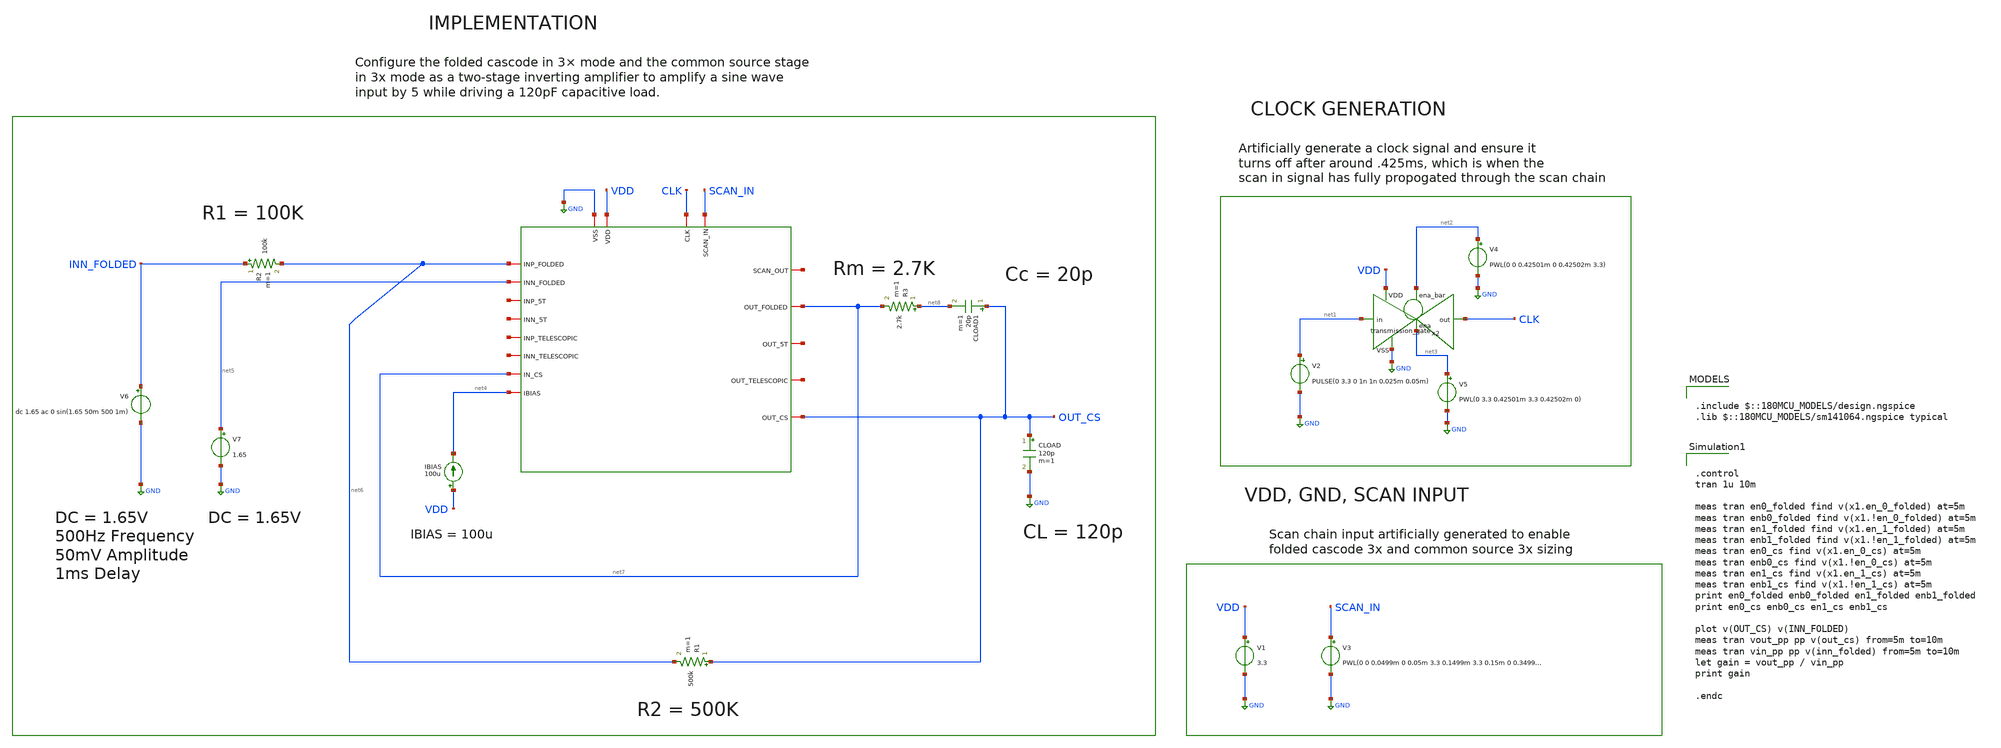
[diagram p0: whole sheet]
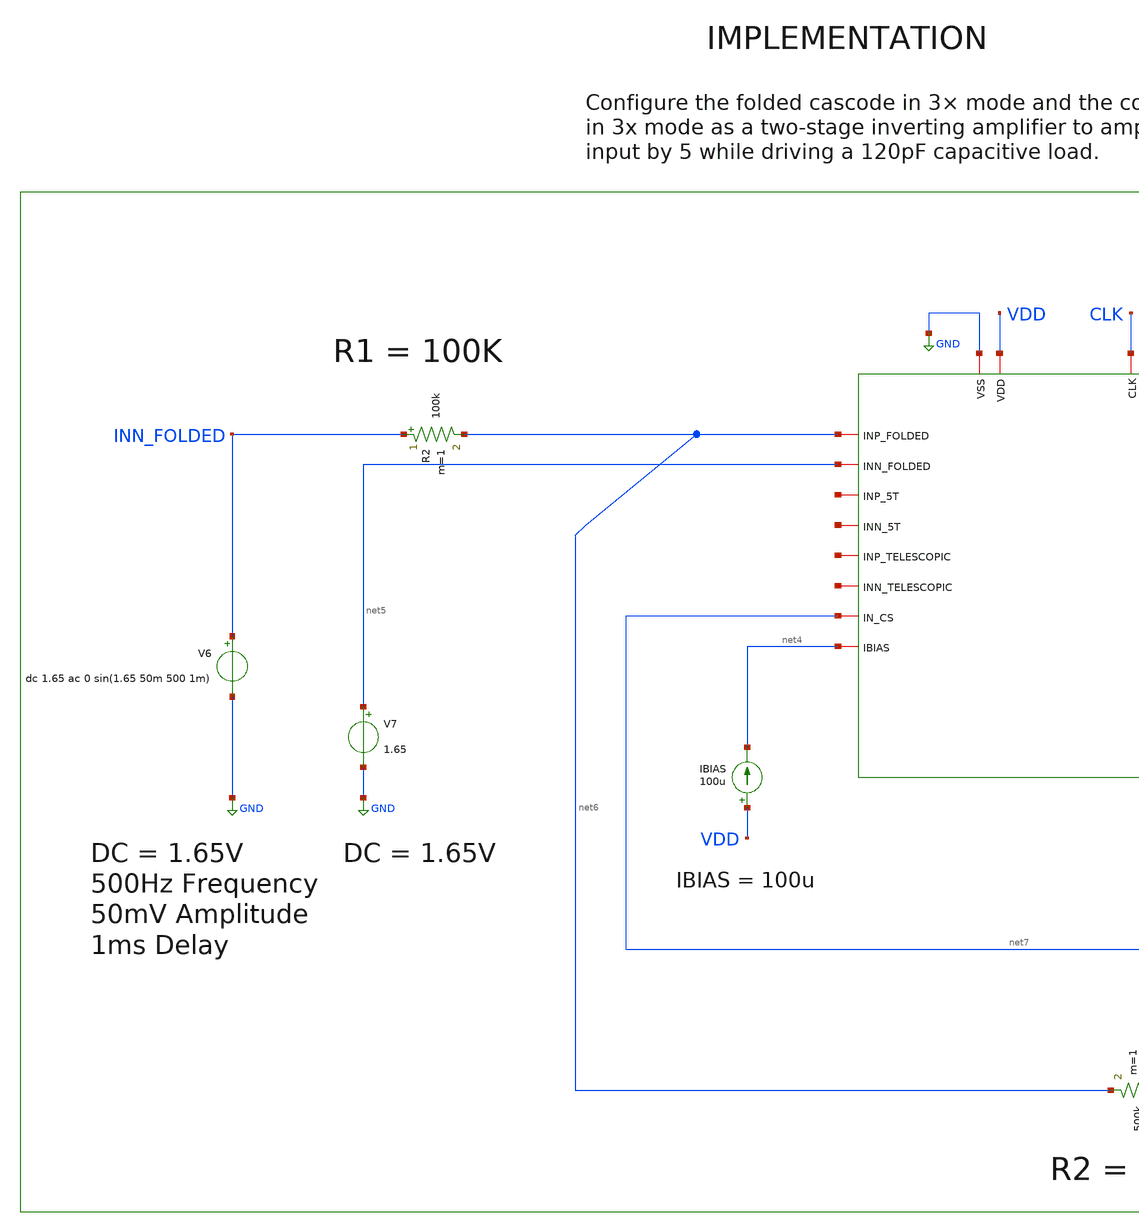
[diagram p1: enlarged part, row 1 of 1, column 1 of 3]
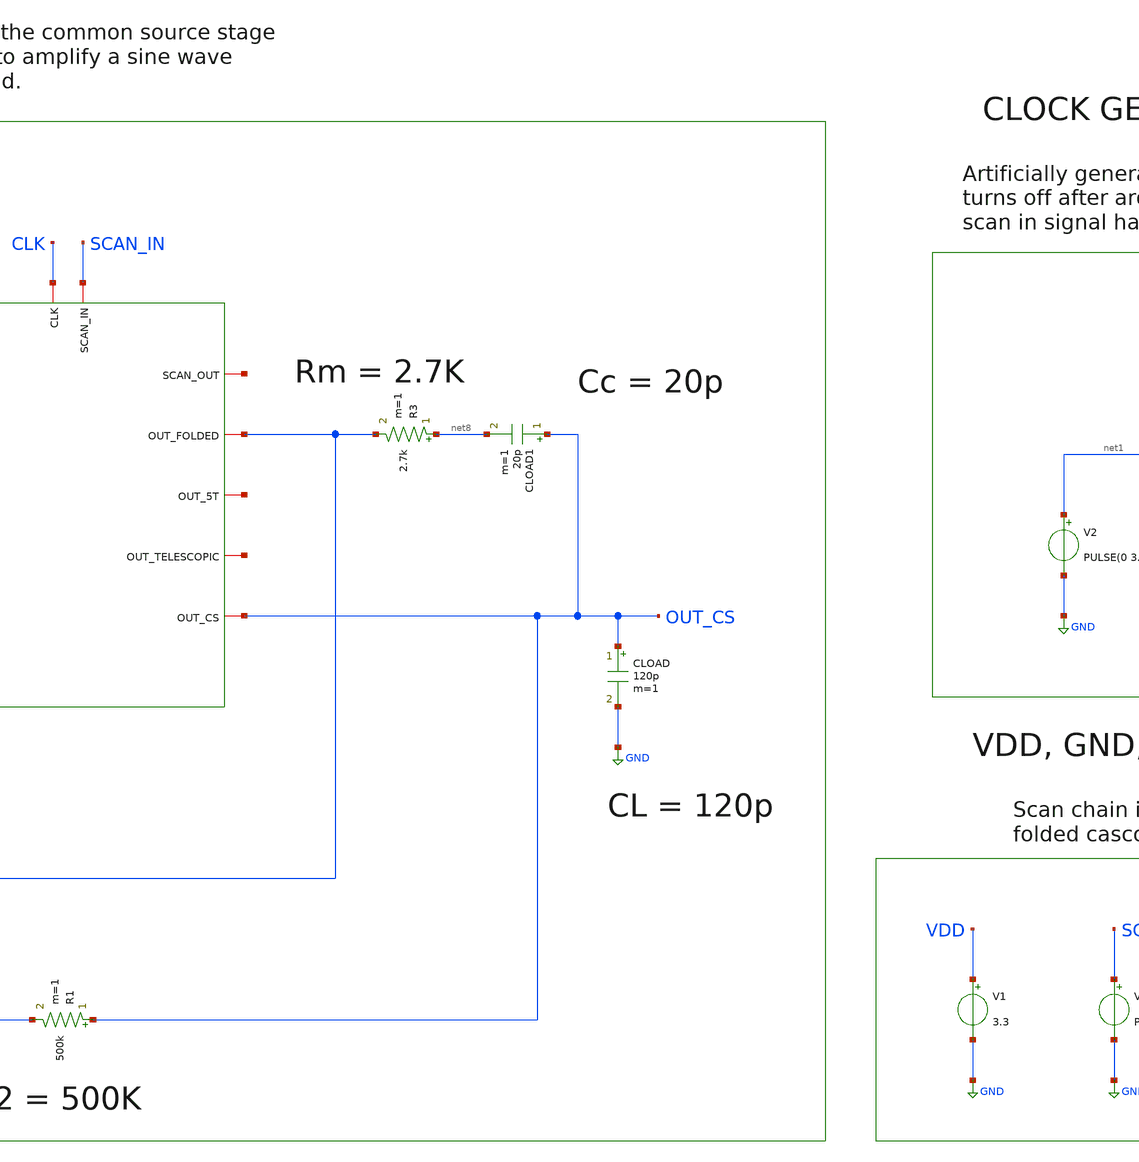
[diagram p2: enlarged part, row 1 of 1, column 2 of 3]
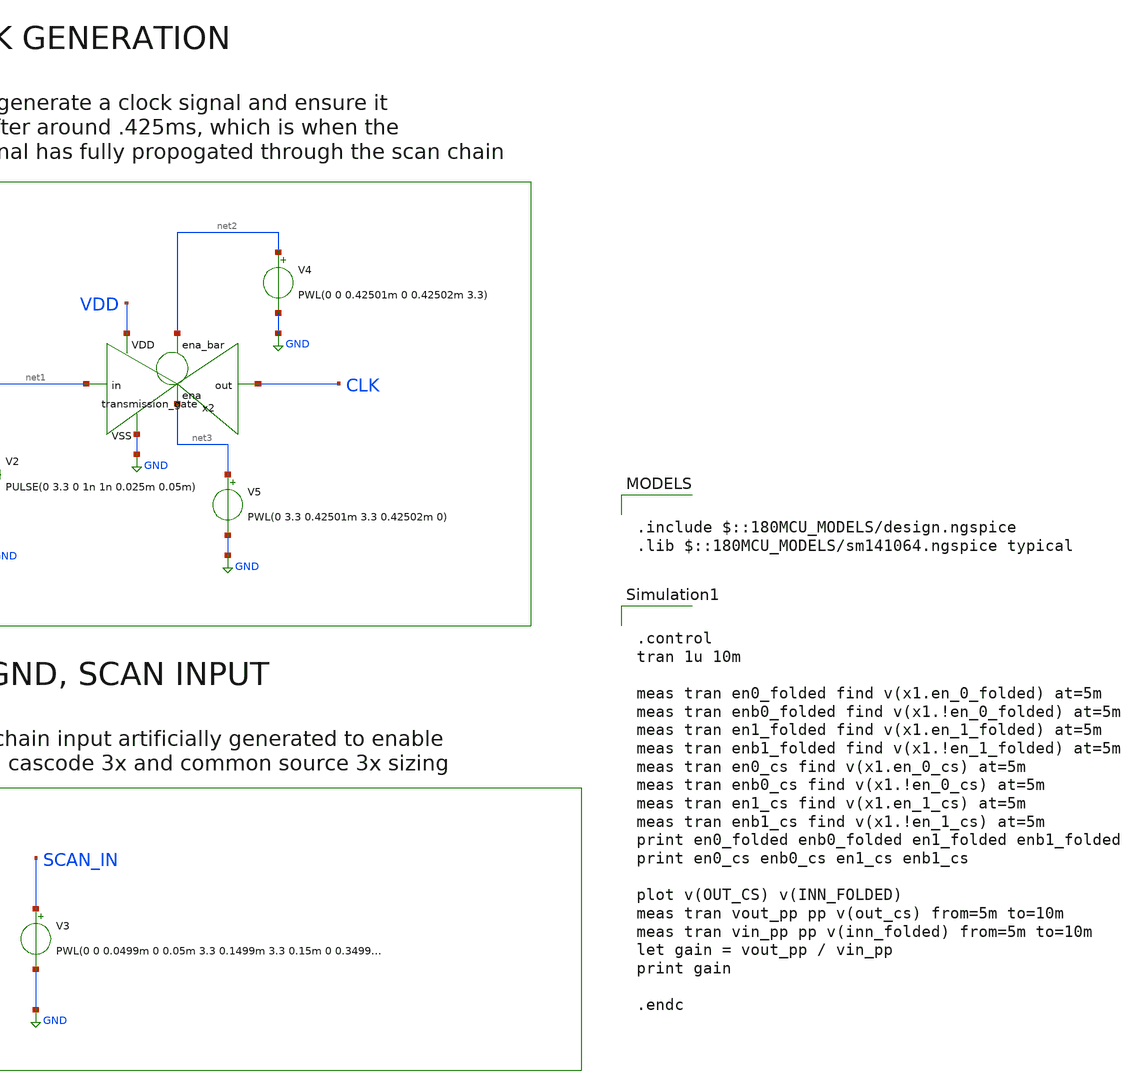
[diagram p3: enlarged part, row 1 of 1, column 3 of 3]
** sch_path: designs/libs/core_tb/etj/ota_folded/two_stage/inverting_amp_3x.sch
**.subckt inverting_amp_3x
V3 SCAN_IN GND PWL(0 0 0.0499m 0 0.05m 3.3 0.1499m 3.3 0.15m 0 0.34999m 0 0.35m 3.3 0.499999m 3.3
+ 0.5m 0)
V1 VDD GND 3.3
V2 net1 GND PULSE(0 3.3 0 1n 1n 0.025m 0.05m)
x2 net2 VDD CLK net1 GND net3 transmission_gate
V4 net2 GND PWL(0 0 0.42501m 0 0.42502m 3.3)
V5 net3 GND PWL(0 3.3 0.42501m 3.3 0.42502m 0)
IBIAS VDD net4 100u
CLOAD OUT_CS GND 120p m=1
R3 net8 net7 2.7k m=1
CLOAD1 OUT_CS net8 20p m=1
V7 net5 GND 1.65
R2 INN_FOLDED net6 100k m=1
R1 OUT_CS net6 500k m=1
V6 INN_FOLDED GND dc 1.65 ac 0 sin(1.65 50m 500 1m)
x1 CLK net9 SCAN_IN GND VDD net7 net6 net10 net4 net5 net11 net12 net13 net14 OUT_CS net7 net15 DUT
**** begin user architecture code

.include $::180MCU_MODELS/design.ngspice
.lib $::180MCU_MODELS/sm141064.ngspice typical



.control
tran 1u 10m

meas tran en0_folded find v(x1.en_0_folded) at=5m
meas tran enb0_folded find v(x1.!en_0_folded) at=5m
meas tran en1_folded find v(x1.en_1_folded) at=5m
meas tran enb1_folded find v(x1.!en_1_folded) at=5m
meas tran en0_cs find v(x1.en_0_cs) at=5m
meas tran enb0_cs find v(x1.!en_0_cs) at=5m
meas tran en1_cs find v(x1.en_1_cs) at=5m
meas tran enb1_cs find v(x1.!en_1_cs) at=5m
print en0_folded enb0_folded en1_folded enb1_folded
print en0_cs enb0_cs en1_cs enb1_cs

plot v(OUT_CS) v(INN_FOLDED)
meas tran vout_pp pp v(out_cs) from=5m to=10m
meas tran vin_pp pp v(inn_folded) from=5m to=10m
let gain = vout_pp / vin_pp
print gain

.endc


**** end user architecture code
**.ends
.GLOBAL GND
.end
